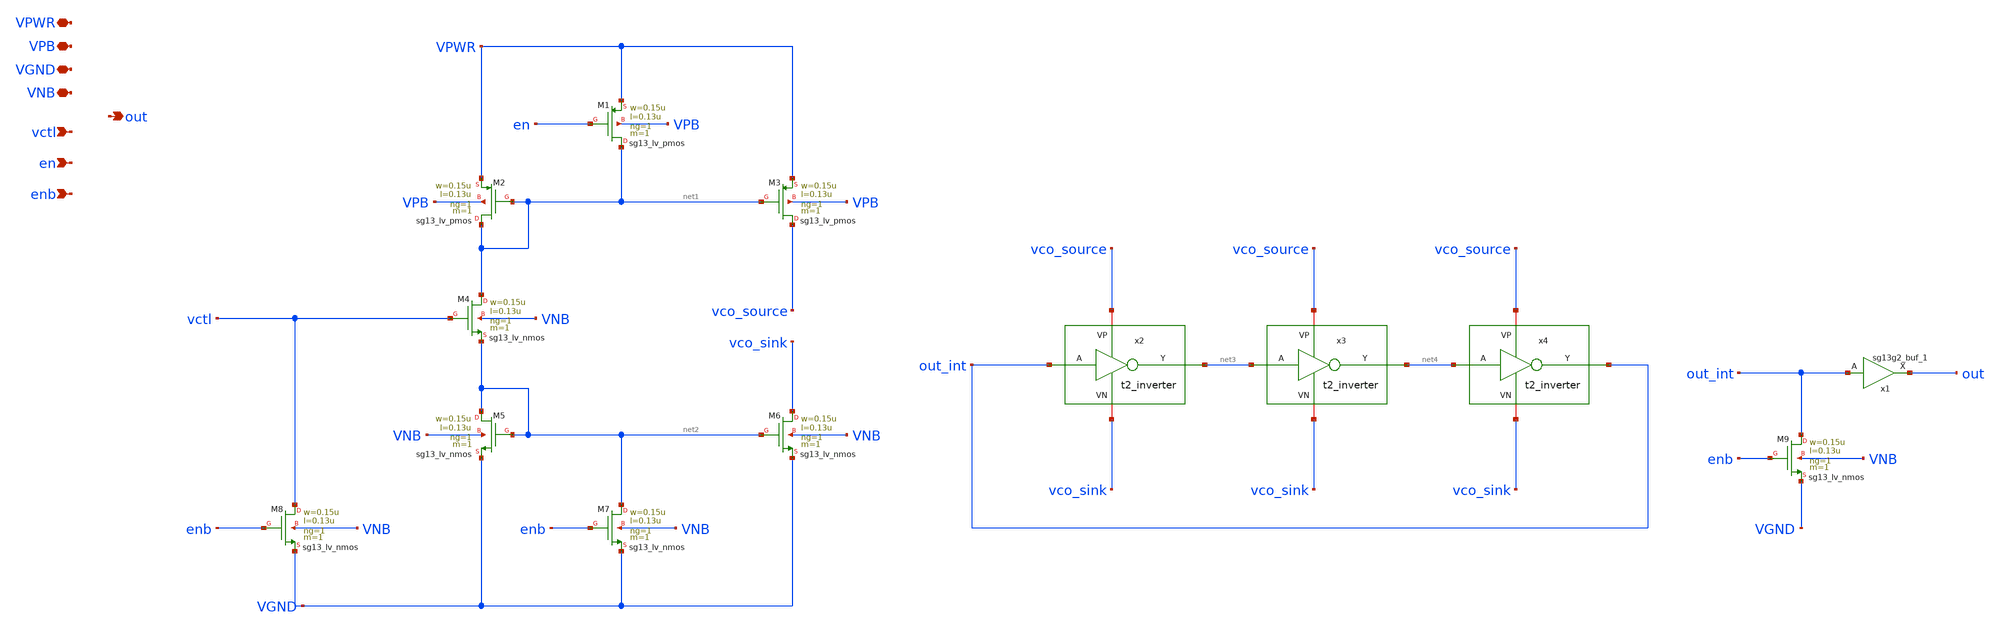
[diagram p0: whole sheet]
** sch_path: Team 2 Design/design_data/xschem/t2_vco.sch
* IHP-GmbH/IHP-Open-PDK/ihp-sg13g2/libs.tech/xschem/sg13g2_stdcells/sg13g2_buf_1.sch:
* Copyright 2023 IHP PDK Authors
* Licensed under the Apache License, Version 2.0 (the "License");
**.subckt t2_vco VPWR VPB VGND VNB vctl en enb out
*.iopin VPWR
*.iopin VPB
*.iopin VGND
*.iopin VNB
*.ipin vctl
*.ipin en
*.ipin enb
*.opin out
XM1 net1 en VPWR VPB sg13_lv_pmos w=0.15u l=0.13u ng=1 m=1 mm_ok=1
XM2 net1 net1 VPWR VPB sg13_lv_pmos w=0.15u l=0.13u ng=1 m=1 mm_ok=1
XM3 vco_source net1 VPWR VPB sg13_lv_pmos w=0.15u l=0.13u ng=1 m=1 mm_ok=1
XM4 net1 vctl net2 VNB sg13_lv_nmos w=0.15u l=0.13u ng=1 m=1 mm_ok=1
XM5 net2 net2 VGND VNB sg13_lv_nmos w=0.15u l=0.13u ng=1 m=1 mm_ok=1
XM6 vco_sink net2 VGND VNB sg13_lv_nmos w=0.15u l=0.13u ng=1 m=1 mm_ok=1
XM7 net2 enb VGND VNB sg13_lv_nmos w=0.15u l=0.13u ng=1 m=1 mm_ok=1
XM8 vctl enb VGND VNB sg13_lv_nmos w=0.15u l=0.13u ng=1 m=1 mm_ok=1
x1 out out_int VDD VSS sg13g2_buf_1
XM9 out_int enb VGND VNB sg13_lv_nmos w=0.15u l=0.13u ng=1 m=1 mm_ok=1
x2 vco_source out_int net3 vco_sink t2_inverter
x3 vco_source net3 net4 vco_sink t2_inverter
x4 vco_source net4 out_int vco_sink t2_inverter
**.ends

* expanding   symbol:  sg13g2_stdcells/sg13g2_buf_1.sym # of pins=2
** sym_path: sg13g2_stdcells/sg13g2_buf_1.sym
** sch_path: sg13g2_stdcells/sg13g2_buf_1.sch
.subckt sg13g2_buf_1 X A VDD VSS
*.ipin A
*.opin X
*.iopin VDD
*.iopin VSS
XM1 net1 A VSS VSS sg13_lv_nmos w=550.00n l=130.00n ng=1 m=1 mm_ok=1
XM2 X net1 VSS VSS sg13_lv_nmos w=740.00n l=130.00n ng=1 m=1 mm_ok=1
XM3 net1 A VDD VDD sg13_lv_pmos w=840.00n l=130.00n ng=1 m=1 mm_ok=1
XM4 X net1 VDD VDD sg13_lv_pmos w=1.12u l=130.00n ng=1 m=1 mm_ok=1
.ends


* expanding   symbol:  /foss/designs/IHP/Inverter/t2_inverter.sym # of pins=4
** sym_path: Team 2 Design/design_data/xschem/t2_inverter.sym
** sch_path: Team 2 Design/design_data/xschem/t2_inverter.sch
.subckt t2_inverter VP A Y VN
*.iopin VP
*.iopin VN
*.ipin A
*.opin Y
XM2 Y A VP VP sg13_lv_pmos w=0.3u l=0.13u ng=1 m=1 mm_ok=1
XM1 Y A VN VN sg13_lv_nmos w=0.15u l=0.13u ng=1 m=1 mm_ok=1
.ends

.end
